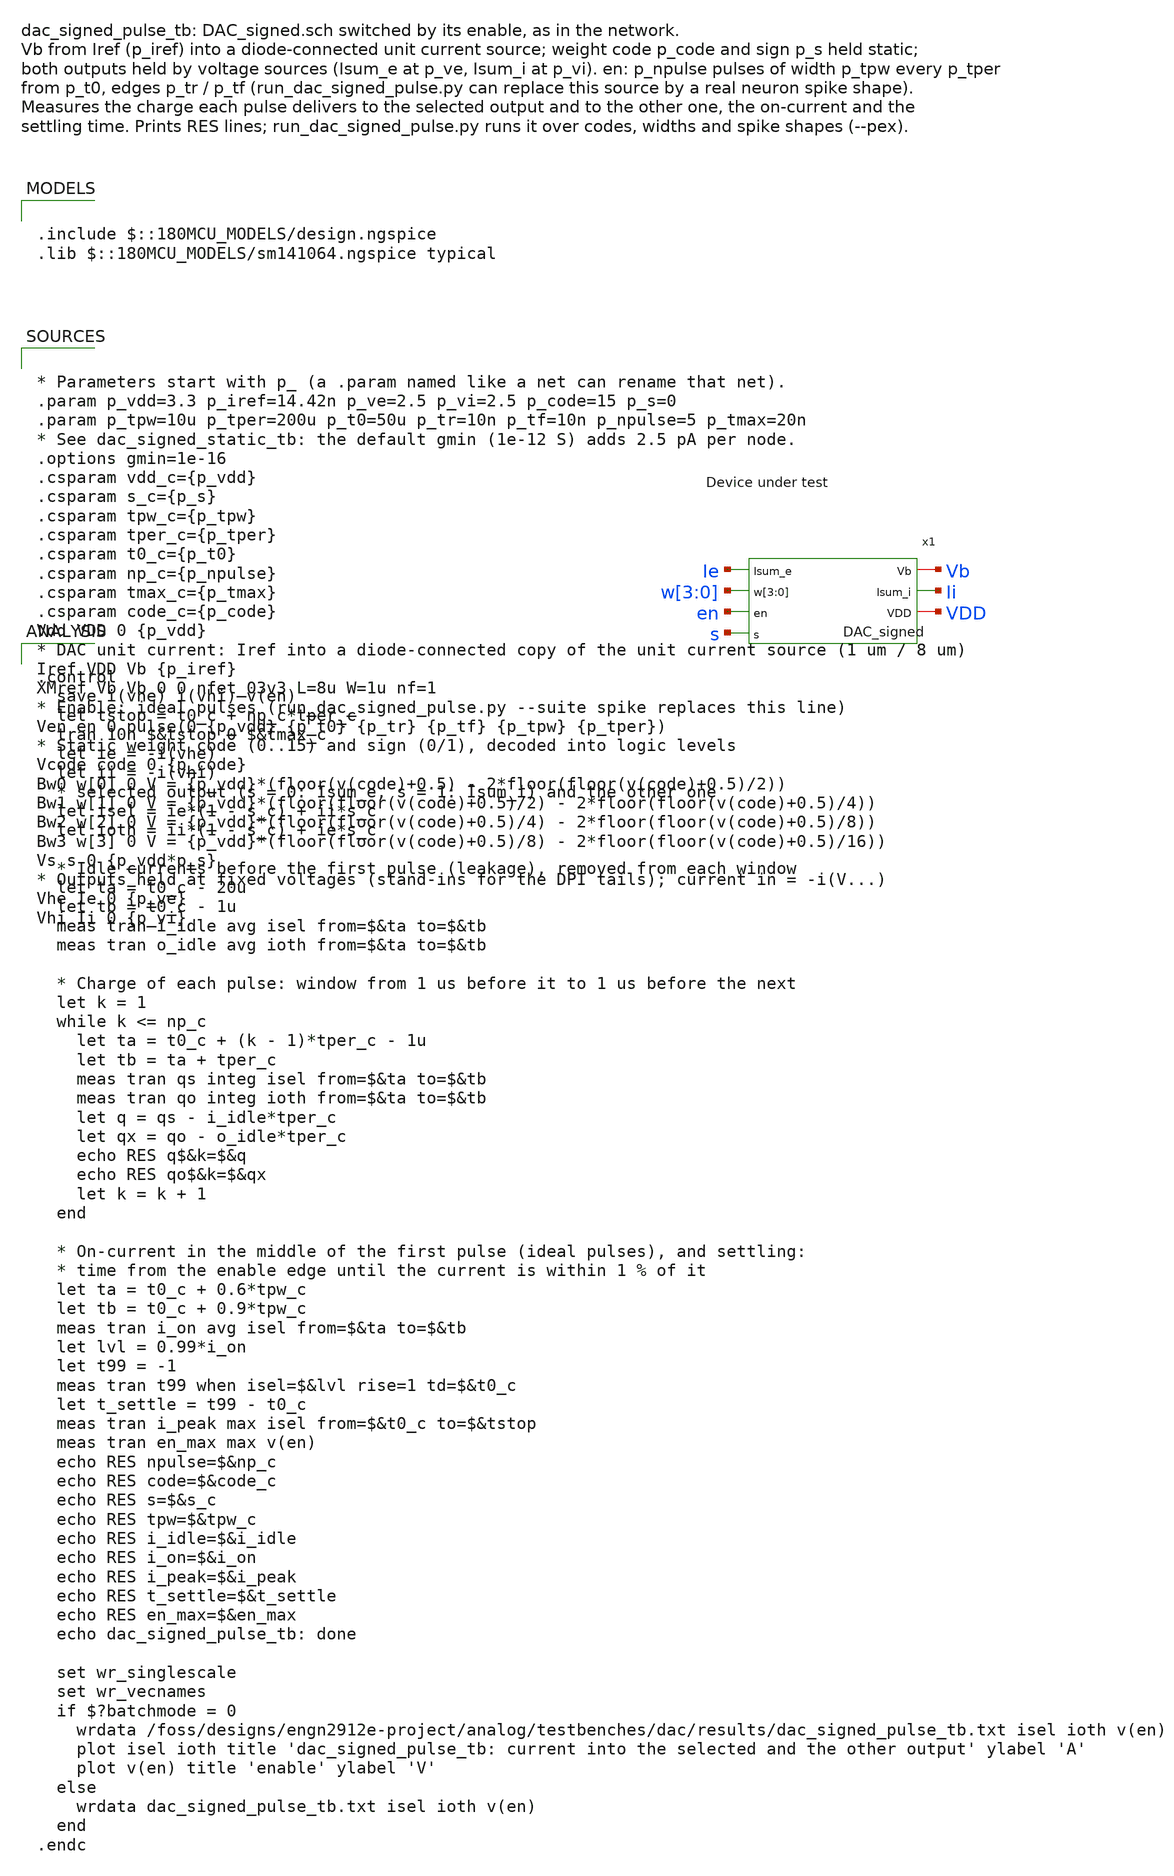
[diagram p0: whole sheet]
** sch_path: analog/testbenches/dac/dac_signed_pulse_tb.sch
**.subckt dac_signed_pulse_tb
x1 Ie w[3] w[2] w[1] w[0] en s Vb Ii VDD DAC_signed
**** begin user architecture code

.include $::180MCU_MODELS/design.ngspice
.lib $::180MCU_MODELS/sm141064.ngspice typical



* Parameters start with p_ (a .param named like a net can rename that net).
.param p_vdd=3.3 p_iref=14.42n p_ve=2.5 p_vi=2.5 p_code=15 p_s=0
.param p_tpw=10u p_tper=200u p_t0=50u p_tr=10n p_tf=10n p_npulse=5 p_tmax=20n
* See dac_signed_static_tb: the default gmin (1e-12 S) adds 2.5 pA per node.
.options gmin=1e-16
.csparam vdd_c={p_vdd}
.csparam s_c={p_s}
.csparam tpw_c={p_tpw}
.csparam tper_c={p_tper}
.csparam t0_c={p_t0}
.csparam np_c={p_npulse}
.csparam tmax_c={p_tmax}
.csparam code_c={p_code}
Vdd VDD 0 {p_vdd}
* DAC unit current: Iref into a diode-connected copy of the unit current source (1 um / 8 um)
Iref VDD Vb {p_iref}
XMref Vb Vb 0 0 nfet_03v3 L=8u W=1u nf=1
* Enable: ideal pulses (run_dac_signed_pulse.py --suite spike replaces this line)
Ven en 0 pulse(0 {p_vdd} {p_t0} {p_tr} {p_tf} {p_tpw} {p_tper})
* Static weight code (0..15) and sign (0/1), decoded into logic levels
Vcode code 0 {p_code}
Bw0 w[0] 0 V = {p_vdd}*(floor(v(code)+0.5) - 2*floor(floor(v(code)+0.5)/2))
Bw1 w[1] 0 V = {p_vdd}*(floor(floor(v(code)+0.5)/2) - 2*floor(floor(v(code)+0.5)/4))
Bw2 w[2] 0 V = {p_vdd}*(floor(floor(v(code)+0.5)/4) - 2*floor(floor(v(code)+0.5)/8))
Bw3 w[3] 0 V = {p_vdd}*(floor(floor(v(code)+0.5)/8) - 2*floor(floor(v(code)+0.5)/16))
Vs s 0 {p_vdd*p_s}
* Outputs held at fixed voltages (stand-ins for the DPI tails); current in = -i(V...)
Vhe Ie 0 {p_ve}
Vhi Ii 0 {p_vi}




.control
  save i(vhe) i(vhi) v(en)
  let tstop = t0_c + np_c*tper_c
  tran 10n $&tstop 0 $&tmax_c
  let ie = -i(vhe)
  let ii = -i(vhi)
  * selected output (s = 0: Isum_e, s = 1: Isum_i) and the other one
  let isel = ie*(1 - s_c) + ii*s_c
  let ioth = ii*(1 - s_c) + ie*s_c

  * Idle currents before the first pulse (leakage), removed from each window
  let ta = t0_c - 20u
  let tb = t0_c - 1u
  meas tran i_idle avg isel from=$&ta to=$&tb
  meas tran o_idle avg ioth from=$&ta to=$&tb

  * Charge of each pulse: window from 1 us before it to 1 us before the next
  let k = 1
  while k <= np_c
    let ta = t0_c + (k - 1)*tper_c - 1u
    let tb = ta + tper_c
    meas tran qs integ isel from=$&ta to=$&tb
    meas tran qo integ ioth from=$&ta to=$&tb
    let q = qs - i_idle*tper_c
    let qx = qo - o_idle*tper_c
    echo RES q$&k=$&q
    echo RES qo$&k=$&qx
    let k = k + 1
  end

  * On-current in the middle of the first pulse (ideal pulses), and settling:
  * time from the enable edge until the current is within 1 % of it
  let ta = t0_c + 0.6*tpw_c
  let tb = t0_c + 0.9*tpw_c
  meas tran i_on avg isel from=$&ta to=$&tb
  let lvl = 0.99*i_on
  let t99 = -1
  meas tran t99 when isel=$&lvl rise=1 td=$&t0_c
  let t_settle = t99 - t0_c
  meas tran i_peak max isel from=$&t0_c to=$&tstop
  meas tran en_max max v(en)
  echo RES npulse=$&np_c
  echo RES code=$&code_c
  echo RES s=$&s_c
  echo RES tpw=$&tpw_c
  echo RES i_idle=$&i_idle
  echo RES i_on=$&i_on
  echo RES i_peak=$&i_peak
  echo RES t_settle=$&t_settle
  echo RES en_max=$&en_max
  echo dac_signed_pulse_tb: done

  set wr_singlescale
  set wr_vecnames
  if $?batchmode = 0
    wrdata /foss/designs/engn2912e-project/analog/testbenches/dac/results/dac_signed_pulse_tb.txt
+ isel ioth v(en)
    plot isel ioth title 'dac_signed_pulse_tb: current into the selected and the other output' ylabel
+ 'A'
    plot v(en) title 'enable' ylabel 'V'
  else
    wrdata dac_signed_pulse_tb.txt isel ioth v(en)
  end
.endc


**** end user architecture code
**.ends

* expanding   symbol:  DAC_signed.sym # of pins=7
** sym_path: analog/neuron/DAC_signed.sym
** sch_path: analog/neuron/DAC_signed.sch
.subckt DAC_signed Isum_e w[3] w[2] w[1] w[0] en s Vb Isum_i VDD
*.ipin w[3],w[2],w[1],w[0]
*.ipin en
*.ipin s
*.iopin Vb
*.iopin VDD
*.iopin Isum_e
*.iopin Isum_i
x1 Y Vb w[3] w[2] w[1] w[0] en DAC
XMse Isum_e sb Y GND nfet_03v3 L=0.28u W=0.22u nf=1 ad='int((nf+1)/2) * W/nf * 0.18u' as='int((nf+2)/2) * W/nf * 0.18u'
+ pd='2*int((nf+1)/2) * (W/nf + 0.18u)' ps='2*int((nf+2)/2) * (W/nf + 0.18u)' nrd='0.18u / W' nrs='0.18u / W'
+ sa=0 sb=0 sd=0 m=1
XMsi Isum_i s Y GND nfet_03v3 L=0.28u W=0.22u nf=1 ad='int((nf+1)/2) * W/nf * 0.18u' as='int((nf+2)/2) * W/nf * 0.18u'
+ pd='2*int((nf+1)/2) * (W/nf + 0.18u)' ps='2*int((nf+2)/2) * (W/nf + 0.18u)' nrd='0.18u / W' nrs='0.18u / W'
+ sa=0 sb=0 sd=0 m=1
XMpi sb s VDD VDD pfet_03v3 L=0.28u W=0.44u nf=1 ad='int((nf+1)/2) * W/nf * 0.18u' as='int((nf+2)/2) * W/nf * 0.18u'
+ pd='2*int((nf+1)/2) * (W/nf + 0.18u)' ps='2*int((nf+2)/2) * (W/nf + 0.18u)' nrd='0.18u / W' nrs='0.18u / W'
+ sa=0 sb=0 sd=0 m=1
XMni sb s GND GND nfet_03v3 L=0.28u W=0.22u nf=1 ad='int((nf+1)/2) * W/nf * 0.18u' as='int((nf+2)/2) * W/nf * 0.18u'
+ pd='2*int((nf+1)/2) * (W/nf + 0.18u)' ps='2*int((nf+2)/2) * (W/nf + 0.18u)' nrd='0.18u / W' nrs='0.18u / W'
+ sa=0 sb=0 sd=0 m=1
.ends


* expanding   symbol:  DAC.sym # of pins=4
** sym_path: analog/neuron/DAC.sym
** sch_path: analog/neuron/DAC.sch
.subckt DAC Isum Vb w[3] w[2] w[1] w[0] en
*.iopin Vb
*.ipin w[3],w[2],w[1],w[0]
*.ipin Isum
*.ipin en
XM1 X w[0] net4 net4 nfet_03v3 L=0.28u W=0.22u nf=1 ad='int((nf+1)/2) * W/nf * 0.18u' as='int((nf+2)/2) * W/nf * 0.18u'
+ pd='2*int((nf+1)/2) * (W/nf + 0.18u)' ps='2*int((nf+2)/2) * (W/nf + 0.18u)' nrd='0.18u / W' nrs='0.18u / W'
+ sa=0 sb=0 sd=0 m=1
XM2 net4 Vb GND GND nfet_03v3 L=8u W=1u nf=1 ad='int((nf+1)/2) * W/nf * 0.18u' as='int((nf+2)/2) * W/nf * 0.18u'
+ pd='2*int((nf+1)/2) * (W/nf + 0.18u)' ps='2*int((nf+2)/2) * (W/nf + 0.18u)' nrd='0.18u / W' nrs='0.18u / W'
+ sa=0 sb=0 sd=0 m=1
XM3 X w[1] net2 net2 nfet_03v3 L=0.28u W=0.22u nf=1 ad='int((nf+1)/2) * W/nf * 0.18u' as='int((nf+2)/2) * W/nf * 0.18u'
+ pd='2*int((nf+1)/2) * (W/nf + 0.18u)' ps='2*int((nf+2)/2) * (W/nf + 0.18u)' nrd='0.18u / W' nrs='0.18u / W'
+ sa=0 sb=0 sd=0 m=2
XM4 net2 Vb GND GND nfet_03v3 L=8u W=1u nf=1 ad='int((nf+1)/2) * W/nf * 0.18u' as='int((nf+2)/2) * W/nf * 0.18u'
+ pd='2*int((nf+1)/2) * (W/nf + 0.18u)' ps='2*int((nf+2)/2) * (W/nf + 0.18u)' nrd='0.18u / W' nrs='0.18u / W'
+ sa=0 sb=0 sd=0 m=2
XM5 X w[2] net3 net3 nfet_03v3 L=0.28u W=0.22u nf=1 ad='int((nf+1)/2) * W/nf * 0.18u' as='int((nf+2)/2) * W/nf * 0.18u'
+ pd='2*int((nf+1)/2) * (W/nf + 0.18u)' ps='2*int((nf+2)/2) * (W/nf + 0.18u)' nrd='0.18u / W' nrs='0.18u / W'
+ sa=0 sb=0 sd=0 m=3
XM6 net3 Vb GND GND nfet_03v3 L=8u W=1u nf=1 ad='int((nf+1)/2) * W/nf * 0.18u' as='int((nf+2)/2) * W/nf * 0.18u'
+ pd='2*int((nf+1)/2) * (W/nf + 0.18u)' ps='2*int((nf+2)/2) * (W/nf + 0.18u)' nrd='0.18u / W' nrs='0.18u / W'
+ sa=0 sb=0 sd=0 m=3
XM7 X w[3] net1 net1 nfet_03v3 L=0.28u W=0.22u nf=1 ad='int((nf+1)/2) * W/nf * 0.18u' as='int((nf+2)/2) * W/nf * 0.18u'
+ pd='2*int((nf+1)/2) * (W/nf + 0.18u)' ps='2*int((nf+2)/2) * (W/nf + 0.18u)' nrd='0.18u / W' nrs='0.18u / W'
+ sa=0 sb=0 sd=0 m=4
XM8 net1 Vb GND GND nfet_03v3 L=8u W=1u nf=1 ad='int((nf+1)/2) * W/nf * 0.18u' as='int((nf+2)/2) * W/nf * 0.18u'
+ pd='2*int((nf+1)/2) * (W/nf + 0.18u)' ps='2*int((nf+2)/2) * (W/nf + 0.18u)' nrd='0.18u / W' nrs='0.18u / W'
+ sa=0 sb=0 sd=0 m=4
XMen Isum en X GND nfet_03v3 L=0.28u W=0.22u nf=1 ad='int((nf+1)/2) * W/nf * 0.18u' as='int((nf+2)/2) * W/nf * 0.18u'
+ pd='2*int((nf+1)/2) * (W/nf + 0.18u)' ps='2*int((nf+2)/2) * (W/nf + 0.18u)' nrd='0.18u / W' nrs='0.18u / W'
+ sa=0 sb=0 sd=0 m=1
.ends

.GLOBAL GND
.end
